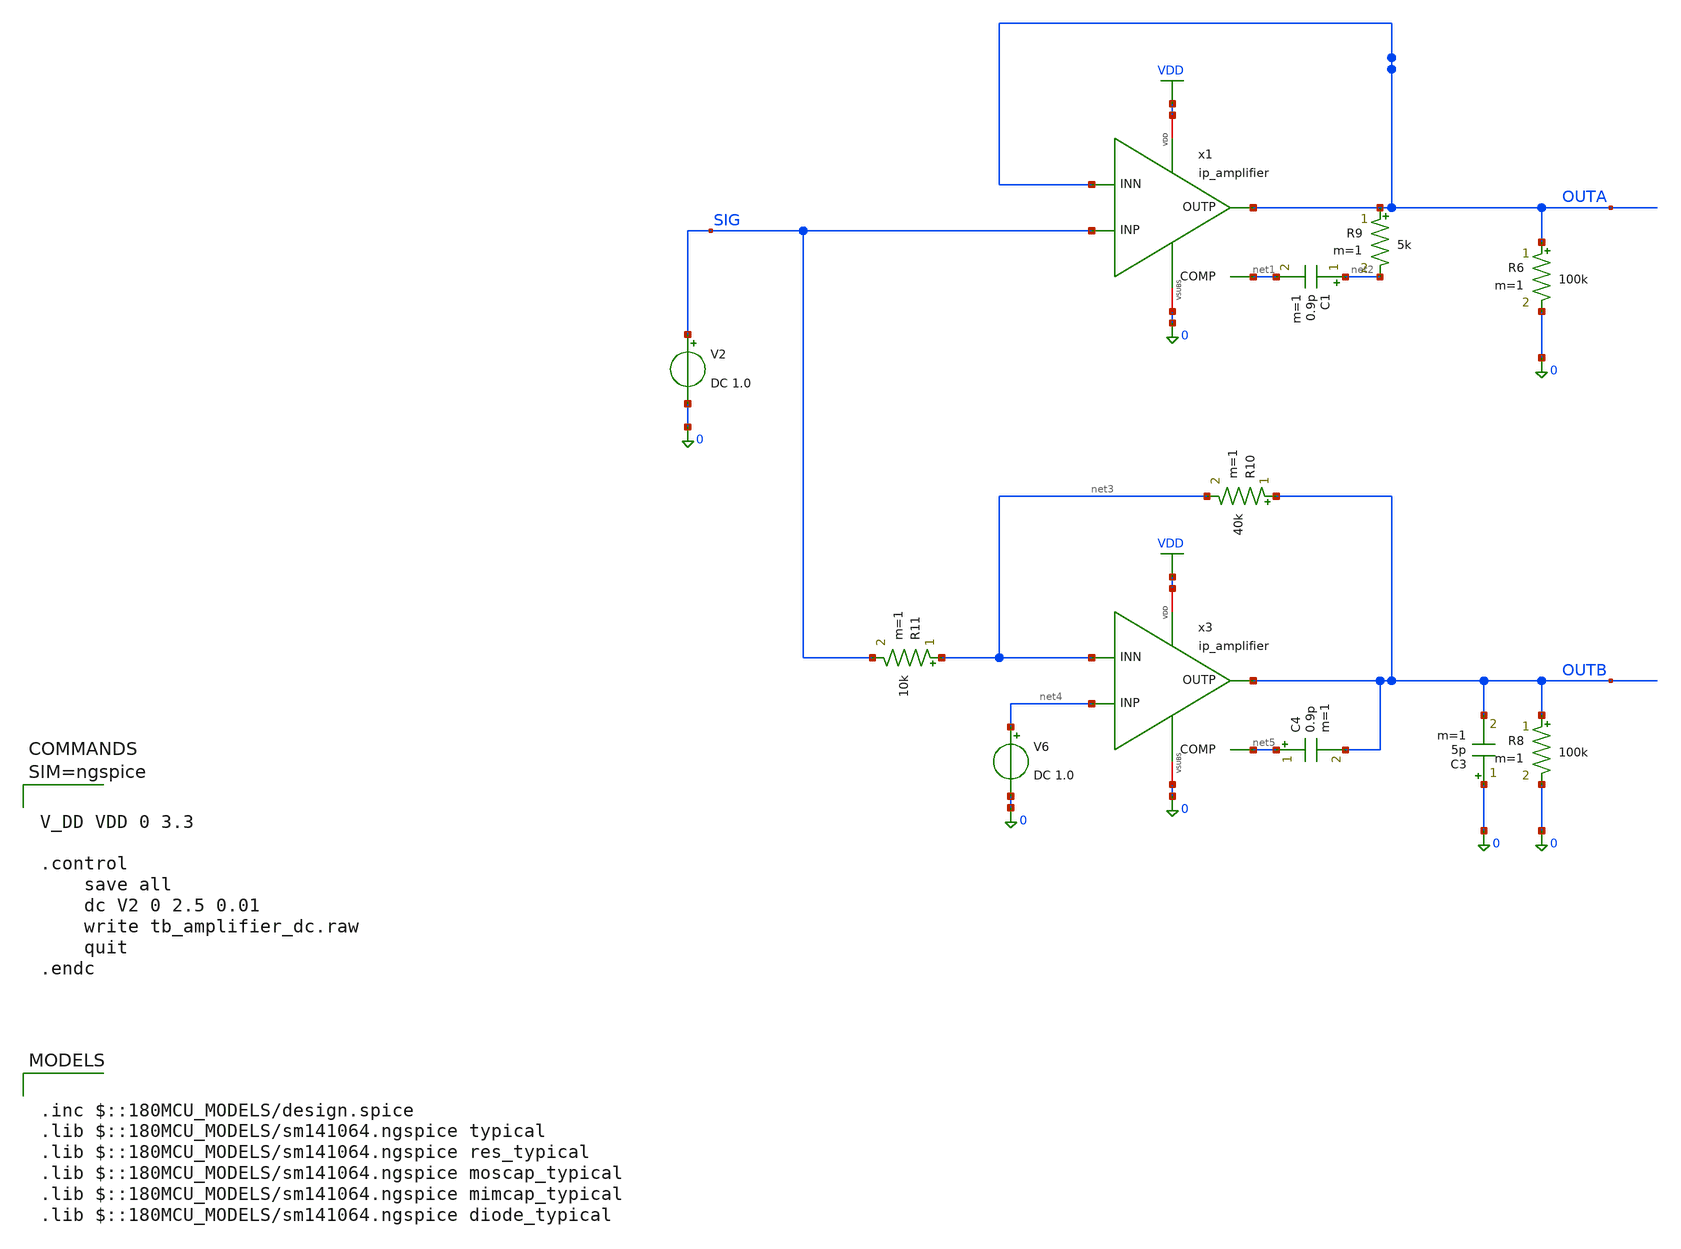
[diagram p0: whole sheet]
** sch_path: xschem/tb_amplifier_dc.sch
**.subckt tb_amplifier_dc
x1 VDD OUTA SIG OUTA 0 net1 ip_amplifier
R6 OUTA 0 100k m=1
x3 VDD OUTB net4 net3 0 net5 ip_amplifier
R8 OUTB 0 100k m=1
C1 net2 net1 0.9p m=1
R9 OUTA net2 5k m=1
R10 OUTB net3 40k m=1
R11 net3 SIG 10k m=1
V6 net4 0 DC 1.0
C3 0 OUTB 5p m=1
C4 net5 OUTB 0.9p m=1
V2 SIG 0 DC 1.0
**** begin user architecture code

.inc $::180MCU_MODELS/design.spice
.lib $::180MCU_MODELS/sm141064.ngspice typical
.lib $::180MCU_MODELS/sm141064.ngspice res_typical
.lib $::180MCU_MODELS/sm141064.ngspice moscap_typical
.lib $::180MCU_MODELS/sm141064.ngspice mimcap_typical
.lib $::180MCU_MODELS/sm141064.ngspice diode_typical




V_DD VDD 0 3.3

.control
	save all
	dc V2 0 2.5 0.01
	write tb_amplifier_dc.raw
	quit
.endc



**** end user architecture code
**.ends

* expanding   symbol:  ip_amplifier.sym # of pins=6
** sym_path: xschem/ip_amplifier.sym
** sch_path: xschem/ip_amplifier.sch
.subckt ip_amplifier VDD OUTP INP INN VSUBS COMP
*.iopin VDD
*.iopin VSUBS
*.ipin INP
*.ipin INN
*.opin OUTP
*.opin COMP
XM1 net10 INP net8 VDD pfet_06v0 L=0.7u W=7.0u nf=1 ad='int((nf+1)/2) * W/nf * 0.18u' as='int((nf+2)/2) * W/nf * 0.18u'
+ pd='2*int((nf+1)/2) * (W/nf + 0.18u)' ps='2*int((nf+2)/2) * (W/nf + 0.18u)' nrd='0.18u / W' nrs='0.18u / W'
+ sa=0 sb=0 sd=0 m=3 par=3
XM2 net9 INN net8 VDD pfet_06v0 L=0.7u W=7.0u nf=1 ad='int((nf+1)/2) * W/nf * 0.18u' as='int((nf+2)/2) * W/nf * 0.18u'
+ pd='2*int((nf+1)/2) * (W/nf + 0.18u)' ps='2*int((nf+2)/2) * (W/nf + 0.18u)' nrd='0.18u / W' nrs='0.18u / W'
+ sa=0 sb=0 sd=0 m=3 par=3
XM5 net10 net1 VSUBS vsubs nfet_06v0 L=2u W=5u nf=1 ad='int((nf+1)/2) * W/nf * 0.18u' as='int((nf+2)/2) * W/nf * 0.18u'
+ pd='2*int((nf+1)/2) * (W/nf + 0.18u)' ps='2*int((nf+2)/2) * (W/nf + 0.18u)' nrd='0.18u / W' nrs='0.18u / W'
+ sa=0 sb=0 sd=0 m=1 par=1
XM6 net9 net1 VSUBS vsubs nfet_06v0 L=2u W=5u nf=1 ad='int((nf+1)/2) * W/nf * 0.18u' as='int((nf+2)/2) * W/nf * 0.18u'
+ pd='2*int((nf+1)/2) * (W/nf + 0.18u)' ps='2*int((nf+2)/2) * (W/nf + 0.18u)' nrd='0.18u / W' nrs='0.18u / W'
+ sa=0 sb=0 sd=0 m=1 par=1
XM3 net3 net1 VSUBS vsubs nfet_06v0 L=1u W=5u nf=1 ad='int((nf+1)/2) * W/nf * 0.18u' as='int((nf+2)/2) * W/nf * 0.18u'
+ pd='2*int((nf+1)/2) * (W/nf + 0.18u)' ps='2*int((nf+2)/2) * (W/nf + 0.18u)' nrd='0.18u / W' nrs='0.18u / W'
+ sa=0 sb=0 sd=0 m=5 par=5
XM4 net2 net1 VSUBS vsubs nfet_06v0 L=1u W=5u nf=1 ad='int((nf+1)/2) * W/nf * 0.18u' as='int((nf+2)/2) * W/nf * 0.18u'
+ pd='2*int((nf+1)/2) * (W/nf + 0.18u)' ps='2*int((nf+2)/2) * (W/nf + 0.18u)' nrd='0.18u / W' nrs='0.18u / W'
+ sa=0 sb=0 sd=0 m=1 par=1
XM7 net1 net1 net3 vsubs nfet_06v0 L=0.7u W=5u nf=1 ad='int((nf+1)/2) * W/nf * 0.18u' as='int((nf+2)/2) * W/nf * 0.18u'
+ pd='2*int((nf+1)/2) * (W/nf + 0.18u)' ps='2*int((nf+2)/2) * (W/nf + 0.18u)' nrd='0.18u / W' nrs='0.18u / W'
+ sa=0 sb=0 sd=0 m=7 par=7
XM8 net4 net1 net2 vsubs nfet_06v0 L=0.7u W=5u nf=1 ad='int((nf+1)/2) * W/nf * 0.18u' as='int((nf+2)/2) * W/nf * 0.18u'
+ pd='2*int((nf+1)/2) * (W/nf + 0.18u)' ps='2*int((nf+2)/2) * (W/nf + 0.18u)' nrd='0.18u / W' nrs='0.18u / W'
+ sa=0 sb=0 sd=0 m=7 par=7
XM9 net5 net7 VDD VDD pfet_06v0 L=1u W=6u nf=1 ad='int((nf+1)/2) * W/nf * 0.18u' as='int((nf+2)/2) * W/nf * 0.18u'
+ pd='2*int((nf+1)/2) * (W/nf + 0.18u)' ps='2*int((nf+2)/2) * (W/nf + 0.18u)' nrd='0.18u / W' nrs='0.18u / W'
+ sa=0 sb=0 sd=0 m=1 par=1
XM10 net6 net7 VDD VDD pfet_06v0 L=1u W=6u nf=1 ad='int((nf+1)/2) * W/nf * 0.18u' as='int((nf+2)/2) * W/nf * 0.18u'
+ pd='2*int((nf+1)/2) * (W/nf + 0.18u)' ps='2*int((nf+2)/2) * (W/nf + 0.18u)' nrd='0.18u / W' nrs='0.18u / W'
+ sa=0 sb=0 sd=0 m=1 par=1
XM11 net7 net7 net5 VDD pfet_06v0 L=0.7u W=7u nf=1 ad='int((nf+1)/2) * W/nf * 0.18u' as='int((nf+2)/2) * W/nf * 0.18u'
+ pd='2*int((nf+1)/2) * (W/nf + 0.18u)' ps='2*int((nf+2)/2) * (W/nf + 0.18u)' nrd='0.18u / W' nrs='0.18u / W'
+ sa=0 sb=0 sd=0 m=5 par=5
XM12 net8 net7 net6 VDD pfet_06v0 L=0.7u W=7u nf=1 ad='int((nf+1)/2) * W/nf * 0.18u' as='int((nf+2)/2) * W/nf * 0.18u'
+ pd='2*int((nf+1)/2) * (W/nf + 0.18u)' ps='2*int((nf+2)/2) * (W/nf + 0.18u)' nrd='0.18u / W' nrs='0.18u / W'
+ sa=0 sb=0 sd=0 m=5 par=5
XM13 net11 net1 net9 vsubs nfet_06v0 L=0.7u W=7u nf=1 ad='int((nf+1)/2) * W/nf * 0.18u' as='int((nf+2)/2) * W/nf * 0.18u'
+ pd='2*int((nf+1)/2) * (W/nf + 0.18u)' ps='2*int((nf+2)/2) * (W/nf + 0.18u)' nrd='0.18u / W' nrs='0.18u / W'
+ sa=0 sb=0 sd=0 m=1 par=1
XM14 COMP net1 net10 vsubs nfet_06v0 L=0.7u W=7u nf=1 ad='int((nf+1)/2) * W/nf * 0.18u' as='int((nf+2)/2) * W/nf * 0.18u'
+ pd='2*int((nf+1)/2) * (W/nf + 0.18u)' ps='2*int((nf+2)/2) * (W/nf + 0.18u)' nrd='0.18u / W' nrs='0.18u / W'
+ sa=0 sb=0 sd=0 m=1 par=1
XM15 net11 net11 VDD VDD pfet_06v0 L=0.7u W=7u nf=1 ad='int((nf+1)/2) * W/nf * 0.18u' as='int((nf+2)/2) * W/nf * 0.18u'
+ pd='2*int((nf+1)/2) * (W/nf + 0.18u)' ps='2*int((nf+2)/2) * (W/nf + 0.18u)' nrd='0.18u / W' nrs='0.18u / W'
+ sa=0 sb=0 sd=0 m=1 par=1
XM16 COMP net11 VDD VDD pfet_06v0 L=0.7u W=7u nf=1 ad='int((nf+1)/2) * W/nf * 0.18u' as='int((nf+2)/2) * W/nf * 0.18u'
+ pd='2*int((nf+1)/2) * (W/nf + 0.18u)' ps='2*int((nf+2)/2) * (W/nf + 0.18u)' nrd='0.18u / W' nrs='0.18u / W'
+ sa=0 sb=0 sd=0 m=1 par=1
XM17 OUTP COMP VDD VDD pfet_06v0 L=0.5u W=5u nf=1 ad='int((nf+1)/2) * W/nf * 0.18u' as='int((nf+2)/2) * W/nf * 0.18u'
+ pd='2*int((nf+1)/2) * (W/nf + 0.18u)' ps='2*int((nf+2)/2) * (W/nf + 0.18u)' nrd='0.18u / W' nrs='0.18u / W'
+ sa=0 sb=0 sd=0 m=12 par=12
XM18 OUTP net10 VSUBS vsubs nfet_06v0 L=0.7u W=5u nf=1 ad='int((nf+1)/2) * W/nf * 0.18u' as='int((nf+2)/2) * W/nf * 0.18u'
+ pd='2*int((nf+1)/2) * (W/nf + 0.18u)' ps='2*int((nf+2)/2) * (W/nf + 0.18u)' nrd='0.18u / W' nrs='0.18u / W'
+ sa=0 sb=0 sd=0 m=6 par=6
XR3 net1 net14 vsubs ppolyf_u_1k_6p0 r_width=1e-6 r_length=6e-6 m=1
XR6 net14 net13 vsubs ppolyf_u_1k_6p0 r_width=1e-6 r_length=6e-6 m=1
XR7 net13 net12 vsubs ppolyf_u_1k_6p0 r_width=1e-6 r_length=6e-6 m=1
XR8 net12 net15 vsubs ppolyf_u_1k_6p0 r_width=1e-6 r_length=4e-6 m=1
Vmeas VDD net15 0
Vmeas1 net7 net4 0
.ends

.GLOBAL VDD
.end
